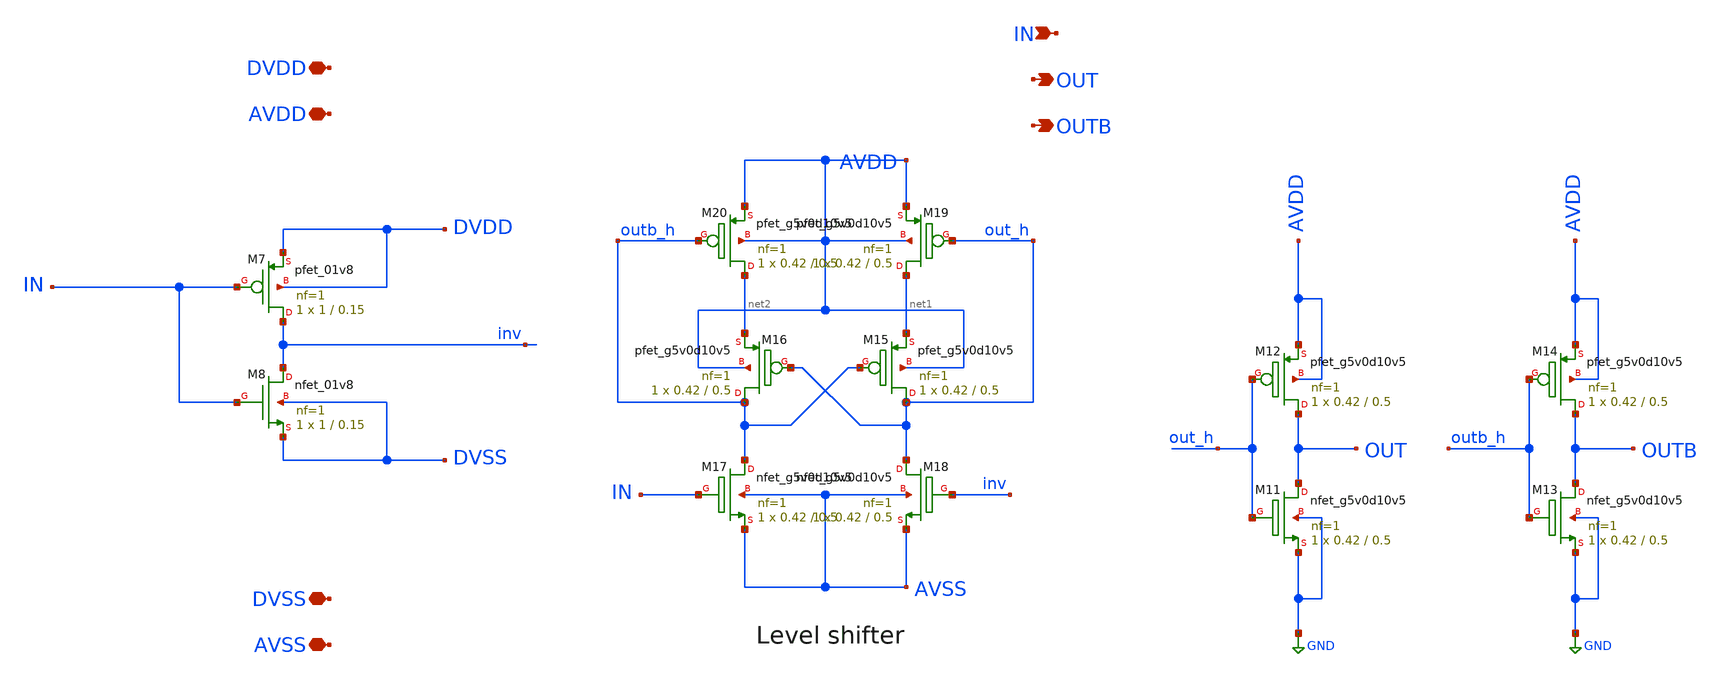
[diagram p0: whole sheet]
** sch_path: level_shifter_gated.sch
**.subckt level_shifter_gated DVDD AVDD DVSS AVSS OUT OUTB IN
*.iopin DVDD
*.iopin AVDD
*.iopin DVSS
*.iopin AVSS
*.opin OUT
*.opin OUTB
*.ipin IN
XM7 inv IN DVDD DVDD sky130_fd_pr__pfet_01v8 L=0.15 W=1 nf=1 ad='int((nf+1)/2) * W/nf * 0.29' as='int((nf+2)/2) * W/nf * 0.29'
+ pd='2*int((nf+1)/2) * (W/nf + 0.29)' ps='2*int((nf+2)/2) * (W/nf + 0.29)' nrd='0.29 / W' nrs='0.29 / W'
+ sa=0 sb=0 sd=0 mult=1 m=1
XM8 inv IN DVSS DVSS sky130_fd_pr__nfet_01v8 L=0.15 W=1 nf=1 ad='int((nf+1)/2) * W/nf * 0.29' as='int((nf+2)/2) * W/nf * 0.29'
+ pd='2*int((nf+1)/2) * (W/nf + 0.29)' ps='2*int((nf+2)/2) * (W/nf + 0.29)' nrd='0.29 / W' nrs='0.29 / W'
+ sa=0 sb=0 sd=0 mult=1 m=1
XM15 out_h outb_h net1 AVDD sky130_fd_pr__pfet_g5v0d10v5 L=0.5 W=0.42 nf=1 ad='int((nf+1)/2) * W/nf * 0.29'
+ as='int((nf+2)/2) * W/nf * 0.29' pd='2*int((nf+1)/2) * (W/nf + 0.29)' ps='2*int((nf+2)/2) * (W/nf + 0.29)'
+ nrd='0.29 / W' nrs='0.29 / W' sa=0 sb=0 sd=0 mult=1 m=1
XM16 outb_h out_h net2 AVDD sky130_fd_pr__pfet_g5v0d10v5 L=0.5 W=0.42 nf=1 ad='int((nf+1)/2) * W/nf * 0.29'
+ as='int((nf+2)/2) * W/nf * 0.29' pd='2*int((nf+1)/2) * (W/nf + 0.29)' ps='2*int((nf+2)/2) * (W/nf + 0.29)'
+ nrd='0.29 / W' nrs='0.29 / W' sa=0 sb=0 sd=0 mult=1 m=1
XM17 outb_h IN AVSS AVSS sky130_fd_pr__nfet_g5v0d10v5 L=0.5 W=0.42 nf=1 ad='int((nf+1)/2) * W/nf * 0.29'
+ as='int((nf+2)/2) * W/nf * 0.29' pd='2*int((nf+1)/2) * (W/nf + 0.29)' ps='2*int((nf+2)/2) * (W/nf + 0.29)'
+ nrd='0.29 / W' nrs='0.29 / W' sa=0 sb=0 sd=0 mult=1 m=1
XM18 out_h inv AVSS AVSS sky130_fd_pr__nfet_g5v0d10v5 L=0.5 W=0.42 nf=1 ad='int((nf+1)/2) * W/nf * 0.29'
+ as='int((nf+2)/2) * W/nf * 0.29' pd='2*int((nf+1)/2) * (W/nf + 0.29)' ps='2*int((nf+2)/2) * (W/nf + 0.29)'
+ nrd='0.29 / W' nrs='0.29 / W' sa=0 sb=0 sd=0 mult=1 m=1
XM19 net1 out_h AVDD AVDD sky130_fd_pr__pfet_g5v0d10v5 L=0.5 W=0.42 nf=1 ad='int((nf+1)/2) * W/nf * 0.29'
+ as='int((nf+2)/2) * W/nf * 0.29' pd='2*int((nf+1)/2) * (W/nf + 0.29)' ps='2*int((nf+2)/2) * (W/nf + 0.29)'
+ nrd='0.29 / W' nrs='0.29 / W' sa=0 sb=0 sd=0 mult=1 m=1
XM20 net2 outb_h AVDD AVDD sky130_fd_pr__pfet_g5v0d10v5 L=0.5 W=0.42 nf=1 ad='int((nf+1)/2) * W/nf * 0.29'
+ as='int((nf+2)/2) * W/nf * 0.29' pd='2*int((nf+1)/2) * (W/nf + 0.29)' ps='2*int((nf+2)/2) * (W/nf + 0.29)'
+ nrd='0.29 / W' nrs='0.29 / W' sa=0 sb=0 sd=0 mult=1 m=1
XM11 OUT out_h GND GND sky130_fd_pr__nfet_g5v0d10v5 L=0.5 W=0.42 nf=1 ad='int((nf+1)/2) * W/nf * 0.29'
+ as='int((nf+2)/2) * W/nf * 0.29' pd='2*int((nf+1)/2) * (W/nf + 0.29)' ps='2*int((nf+2)/2) * (W/nf + 0.29)'
+ nrd='0.29 / W' nrs='0.29 / W' sa=0 sb=0 sd=0 mult=1 m=1
XM12 OUT out_h AVDD AVDD sky130_fd_pr__pfet_g5v0d10v5 L=0.5 W=0.42 nf=1 ad='int((nf+1)/2) * W/nf * 0.29'
+ as='int((nf+2)/2) * W/nf * 0.29' pd='2*int((nf+1)/2) * (W/nf + 0.29)' ps='2*int((nf+2)/2) * (W/nf + 0.29)'
+ nrd='0.29 / W' nrs='0.29 / W' sa=0 sb=0 sd=0 mult=1 m=1
XM13 OUTB outb_h GND GND sky130_fd_pr__nfet_g5v0d10v5 L=0.5 W=0.42 nf=1 ad='int((nf+1)/2) * W/nf * 0.29'
+ as='int((nf+2)/2) * W/nf * 0.29' pd='2*int((nf+1)/2) * (W/nf + 0.29)' ps='2*int((nf+2)/2) * (W/nf + 0.29)'
+ nrd='0.29 / W' nrs='0.29 / W' sa=0 sb=0 sd=0 mult=1 m=1
XM14 OUTB outb_h AVDD AVDD sky130_fd_pr__pfet_g5v0d10v5 L=0.5 W=0.42 nf=1 ad='int((nf+1)/2) * W/nf * 0.29'
+ as='int((nf+2)/2) * W/nf * 0.29' pd='2*int((nf+1)/2) * (W/nf + 0.29)' ps='2*int((nf+2)/2) * (W/nf + 0.29)'
+ nrd='0.29 / W' nrs='0.29 / W' sa=0 sb=0 sd=0 mult=1 m=1
**.ends
.GLOBAL GND
.end
